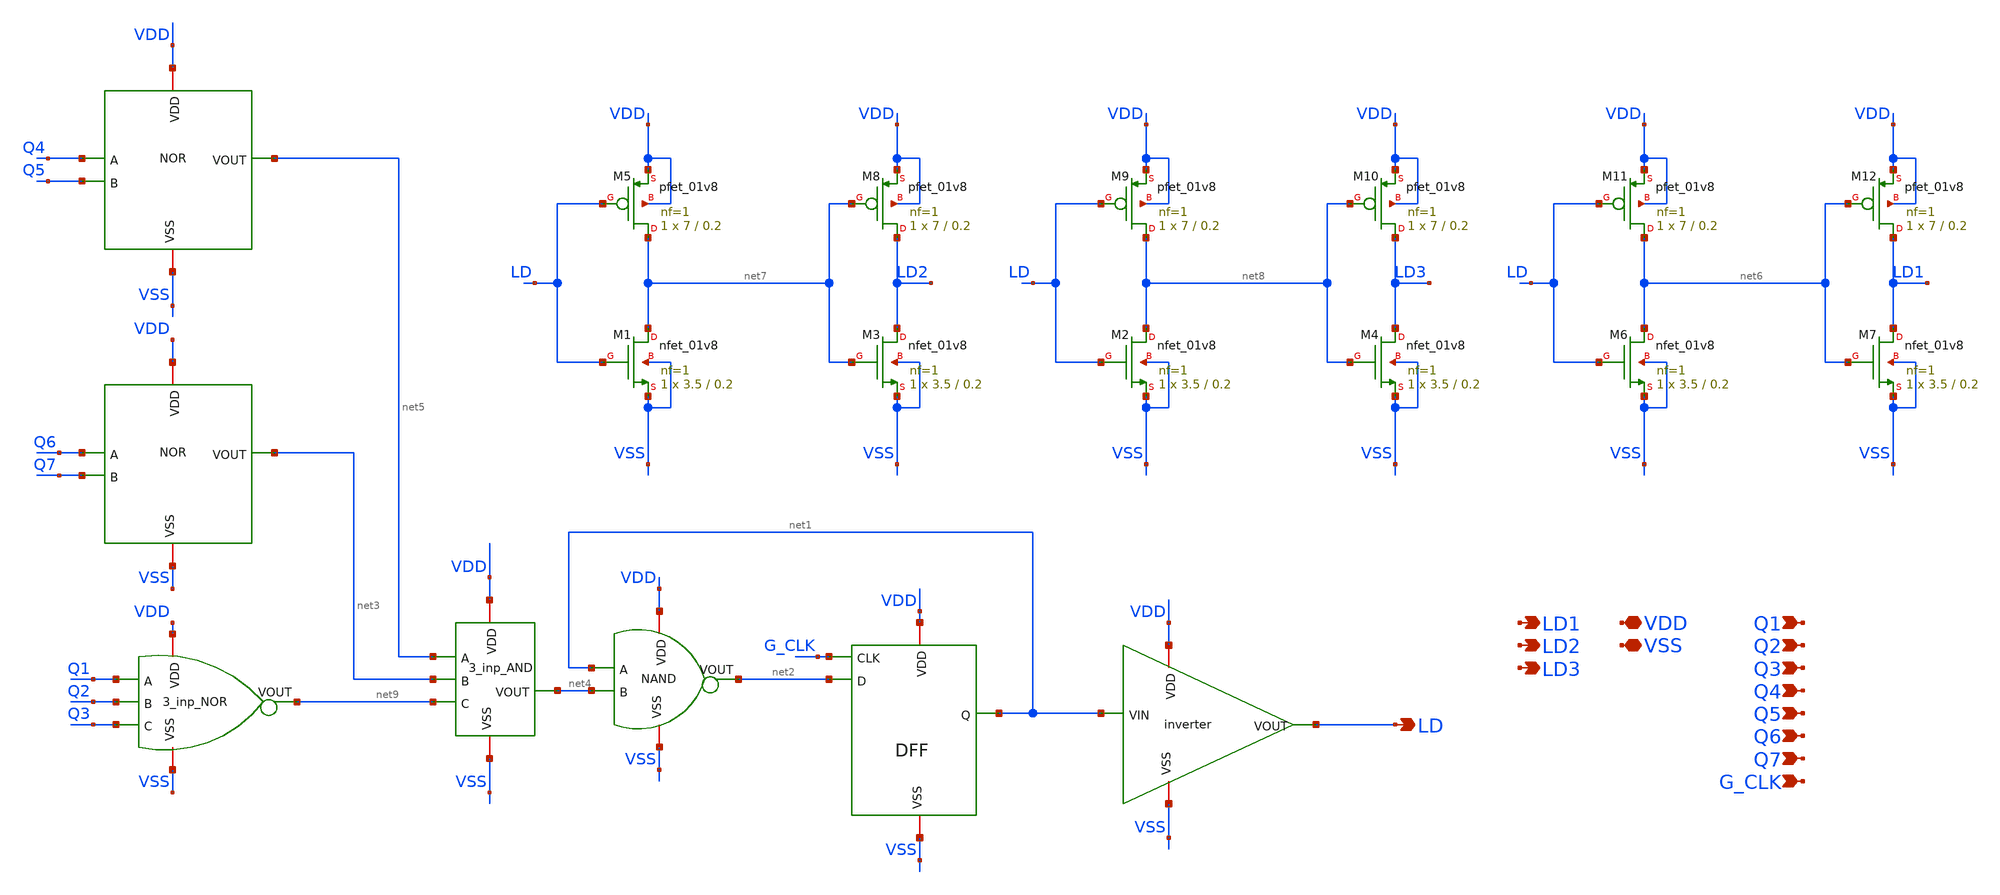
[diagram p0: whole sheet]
** sch_path: Xschem/PLL_TOP_Schematics/LD_GENERATOR.sch
**.subckt LD_GENERATOR LD LD1 LD2 LD3 VDD VSS Q1 Q2 Q3 Q4 Q5 Q6 Q7 G_CLK
*.opin LD
*.opin LD1
*.opin LD2
*.opin LD3
*.iopin VDD
*.iopin VSS
*.ipin Q1
*.ipin Q2
*.ipin Q3
*.ipin Q4
*.ipin Q5
*.ipin Q6
*.ipin Q7
*.ipin G_CLK
x6 VDD net2 net1 net4 VSS NAND
x9 VDD Q1 Q2 Q3 net9 VSS 3_inp_NOR
x7 G_CLK VDD net2 net1 VSS DFF
x8 VDD net1 LD VSS inverter
x5 VDD net4 net5 net3 net9 VSS 3_inp_AND
x13 VDD Q4 Q5 net5 VSS NOR
x14 VDD Q6 Q7 net3 VSS NOR
XM5 net7 LD VDD VDD sky130_fd_pr__pfet_01v8 L=0.2 W=7 nf=1 ad='int((nf+1)/2) * W/nf * 0.29' as='int((nf+2)/2) * W/nf * 0.29'
+ pd='2*int((nf+1)/2) * (W/nf + 0.29)' ps='2*int((nf+2)/2) * (W/nf + 0.29)' nrd='0.29 / W' nrs='0.29 / W'
+ sa=0 sb=0 sd=0 mult=1 m=1
XM2 net8 LD VSS VSS sky130_fd_pr__nfet_01v8 L=0.2 W=3.5 nf=1 ad='int((nf+1)/2) * W/nf * 0.29' as='int((nf+2)/2) * W/nf * 0.29'
+ pd='2*int((nf+1)/2) * (W/nf + 0.29)' ps='2*int((nf+2)/2) * (W/nf + 0.29)' nrd='0.29 / W' nrs='0.29 / W'
+ sa=0 sb=0 sd=0 mult=1 m=1
XM1 net7 LD VSS VSS sky130_fd_pr__nfet_01v8 L=0.2 W=3.5 nf=1 ad='int((nf+1)/2) * W/nf * 0.29' as='int((nf+2)/2) * W/nf * 0.29'
+ pd='2*int((nf+1)/2) * (W/nf + 0.29)' ps='2*int((nf+2)/2) * (W/nf + 0.29)' nrd='0.29 / W' nrs='0.29 / W'
+ sa=0 sb=0 sd=0 mult=1 m=1
XM3 LD2 net7 VSS VSS sky130_fd_pr__nfet_01v8 L=0.2 W=3.5 nf=1 ad='int((nf+1)/2) * W/nf * 0.29' as='int((nf+2)/2) * W/nf * 0.29'
+ pd='2*int((nf+1)/2) * (W/nf + 0.29)' ps='2*int((nf+2)/2) * (W/nf + 0.29)' nrd='0.29 / W' nrs='0.29 / W'
+ sa=0 sb=0 sd=0 mult=1 m=1
XM4 LD3 net8 VSS VSS sky130_fd_pr__nfet_01v8 L=0.2 W=3.5 nf=1 ad='int((nf+1)/2) * W/nf * 0.29' as='int((nf+2)/2) * W/nf * 0.29'
+ pd='2*int((nf+1)/2) * (W/nf + 0.29)' ps='2*int((nf+2)/2) * (W/nf + 0.29)' nrd='0.29 / W' nrs='0.29 / W'
+ sa=0 sb=0 sd=0 mult=1 m=1
XM6 net6 LD VSS VSS sky130_fd_pr__nfet_01v8 L=0.2 W=3.5 nf=1 ad='int((nf+1)/2) * W/nf * 0.29' as='int((nf+2)/2) * W/nf * 0.29'
+ pd='2*int((nf+1)/2) * (W/nf + 0.29)' ps='2*int((nf+2)/2) * (W/nf + 0.29)' nrd='0.29 / W' nrs='0.29 / W'
+ sa=0 sb=0 sd=0 mult=1 m=1
XM7 LD1 net6 VSS VSS sky130_fd_pr__nfet_01v8 L=0.2 W=3.5 nf=1 ad='int((nf+1)/2) * W/nf * 0.29' as='int((nf+2)/2) * W/nf * 0.29'
+ pd='2*int((nf+1)/2) * (W/nf + 0.29)' ps='2*int((nf+2)/2) * (W/nf + 0.29)' nrd='0.29 / W' nrs='0.29 / W'
+ sa=0 sb=0 sd=0 mult=1 m=1
XM8 LD2 net7 VDD VDD sky130_fd_pr__pfet_01v8 L=0.2 W=7 nf=1 ad='int((nf+1)/2) * W/nf * 0.29' as='int((nf+2)/2) * W/nf * 0.29'
+ pd='2*int((nf+1)/2) * (W/nf + 0.29)' ps='2*int((nf+2)/2) * (W/nf + 0.29)' nrd='0.29 / W' nrs='0.29 / W'
+ sa=0 sb=0 sd=0 mult=1 m=1
XM9 net8 LD VDD VDD sky130_fd_pr__pfet_01v8 L=0.2 W=7 nf=1 ad='int((nf+1)/2) * W/nf * 0.29' as='int((nf+2)/2) * W/nf * 0.29'
+ pd='2*int((nf+1)/2) * (W/nf + 0.29)' ps='2*int((nf+2)/2) * (W/nf + 0.29)' nrd='0.29 / W' nrs='0.29 / W'
+ sa=0 sb=0 sd=0 mult=1 m=1
XM10 LD3 net8 VDD VDD sky130_fd_pr__pfet_01v8 L=0.2 W=7 nf=1 ad='int((nf+1)/2) * W/nf * 0.29' as='int((nf+2)/2) * W/nf * 0.29'
+ pd='2*int((nf+1)/2) * (W/nf + 0.29)' ps='2*int((nf+2)/2) * (W/nf + 0.29)' nrd='0.29 / W' nrs='0.29 / W'
+ sa=0 sb=0 sd=0 mult=1 m=1
XM11 net6 LD VDD VDD sky130_fd_pr__pfet_01v8 L=0.2 W=7 nf=1 ad='int((nf+1)/2) * W/nf * 0.29' as='int((nf+2)/2) * W/nf * 0.29'
+ pd='2*int((nf+1)/2) * (W/nf + 0.29)' ps='2*int((nf+2)/2) * (W/nf + 0.29)' nrd='0.29 / W' nrs='0.29 / W'
+ sa=0 sb=0 sd=0 mult=1 m=1
XM12 LD1 net6 VDD VDD sky130_fd_pr__pfet_01v8 L=0.2 W=7 nf=1 ad='int((nf+1)/2) * W/nf * 0.29' as='int((nf+2)/2) * W/nf * 0.29'
+ pd='2*int((nf+1)/2) * (W/nf + 0.29)' ps='2*int((nf+2)/2) * (W/nf + 0.29)' nrd='0.29 / W' nrs='0.29 / W'
+ sa=0 sb=0 sd=0 mult=1 m=1
**.ends
.end
